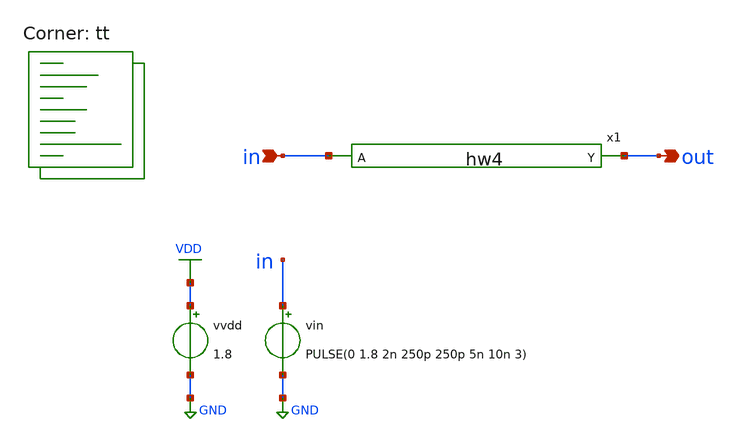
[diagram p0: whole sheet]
** sch_path: xschem/sim/tb_hw4.sch
**.subckt tb_hw4 in out
*.ipin in
*.opin out
vvdd VDD GND 1.8
vin in GND PULSE(0 1.8 2n 250p 250p 5n 10n 3)
x1 in out hw4
**** begin user architecture code
.lib $::SKYWATER_MODELS/sky130.lib.spice tt


.control
* VTC analysis
DC vin 0 1.8 1m
save all
let VP = 1.8
let vo_mid = VP/2
let dvout = deriv(v(out))
meas DC VSW find v(in) when v(out)=vo_mid
meas DC VIL find v(in) WHEN dvout=-1 CROSS=1
meas DC VIH find v(in) WHEN dvout=-1 CROSS=2
meas DC VOL find v(out) WHEN dvout=-1 CROSS=2
meas DC VOH find v(out) WHEN dvout=-1 CROSS=1
echo VTC measurements
print VSW
print VIL
print VIH
print VOH
print VOL
print v(in) v(out) deriv(v(out))
echo
set filetype=binary
write tb_inv_vtc.raw v(out) v(in) dvout VSW VIL VIH VOH VOL

* Transient analysis
TRAN 1p 40n
save all
let VP=1.8
let per10 = Vp*0.1
let per50 = Vp*0.5
let per90 = Vp*0.9
meas TRAN t_rise  TRIG v(out) VAL=per10 rise=1  TARG v(out) VAL=per90 rise=1
meas TRAN t_fall  TRIG v(out) VAL=per90 fall=1  TARG v(out) VAL=per10 fall=1
meas TRAN t_delay  TRIG v(in) VAL=per50 rise=1 TARG v(out) VAL=per50 fall=1
echo TRAN measurements
print t_delay
print t_rise
print t_fall
echo
set filetype=binary
write tb_inv_tran.raw
.endc


**** end user architecture code
**.ends

* expanding   symbol:  hw4.sym # of pins=2
** sym_path: xschem/sim/hw4.sym
** sch_path: xschem/sim/hw4.sch
.subckt hw4 A Y
*.opin Y
*.ipin A
XM1 Y A VDD VDD sky130_fd_pr__pfet_01v8 L=0.15 W=0.84 nf=1 ad='int((nf+1)/2) * W/nf * 0.29' as='int((nf+2)/2) * W/nf * 0.29'
+ pd='2*int((nf+1)/2) * (W/nf + 0.29)' ps='2*int((nf+2)/2) * (W/nf + 0.29)' nrd='0.29 / W' nrs='0.29 / W'
+ sa=0 sb=0 sd=0 mult=1 m=1
XM2 Y A GND GND sky130_fd_pr__nfet_01v8 L=0.15 W=0.42 nf=1 ad='int((nf+1)/2) * W/nf * 0.29' as='int((nf+2)/2) * W/nf * 0.29'
+ pd='2*int((nf+1)/2) * (W/nf + 0.29)' ps='2*int((nf+2)/2) * (W/nf + 0.29)' nrd='0.29 / W' nrs='0.29 / W'
+ sa=0 sb=0 sd=0 mult=1 m=1
.ends

.GLOBAL GND
.GLOBAL VDD
.end
